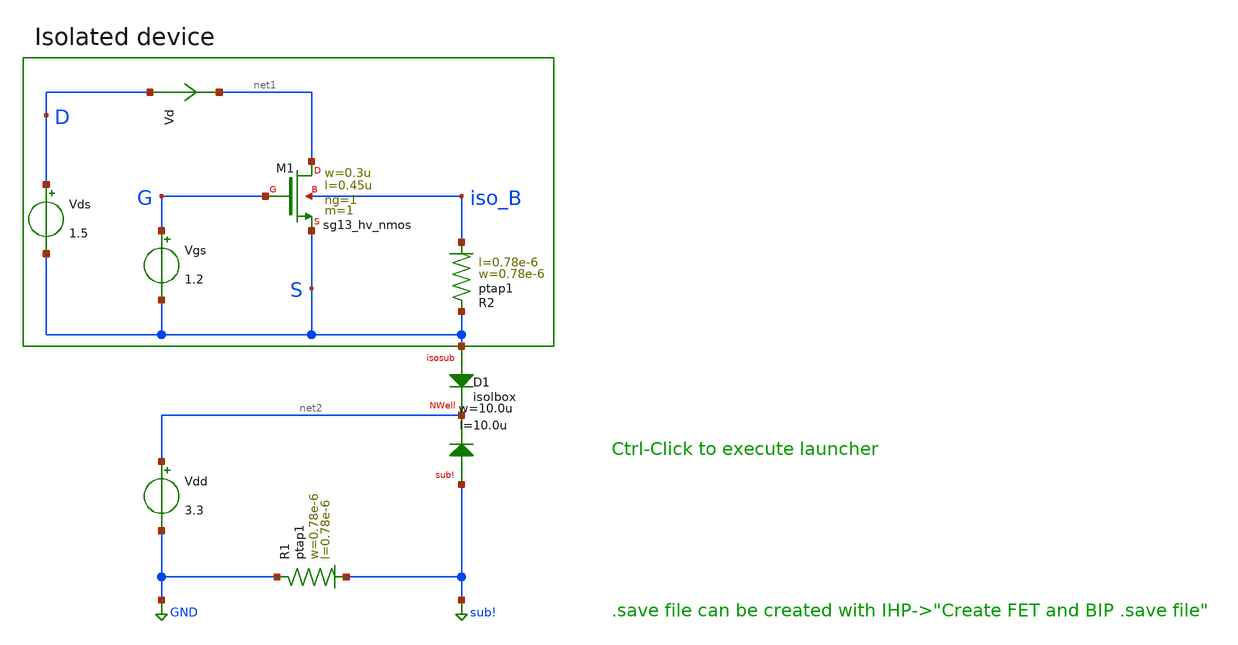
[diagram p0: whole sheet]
** sch_path: ihp-sg13g2/xschem_libs/sg13g2_tests_ase/iso_dc_hv_nmos/schematic/iso_dc_hv_nmos.sch
* Copyright 2023 IHP PDK Authors
**.subckt iso_dc_hv_nmos
Vgs G S 1.2
Vds D S 1.5
Vd D net1 0
.save i(vd)
XD1 S net2 sub! isolbox l=10.0u w=10.0u
XR1 GND sub! ptap1 R=262.8 w=0.78e-6 l=0.78e-6
XR2 S iso_B ptap1 R=262.8 w=0.78e-6 l=0.78e-6
Vdd net2 GND 3.3
XM1 net1 G S iso_B sg13_hv_nmos w=0.3u l=0.45u ng=1 m=1 mm_ok=1
**.ends
.GLOBAL GND
.GLOBAL sub!
.end
